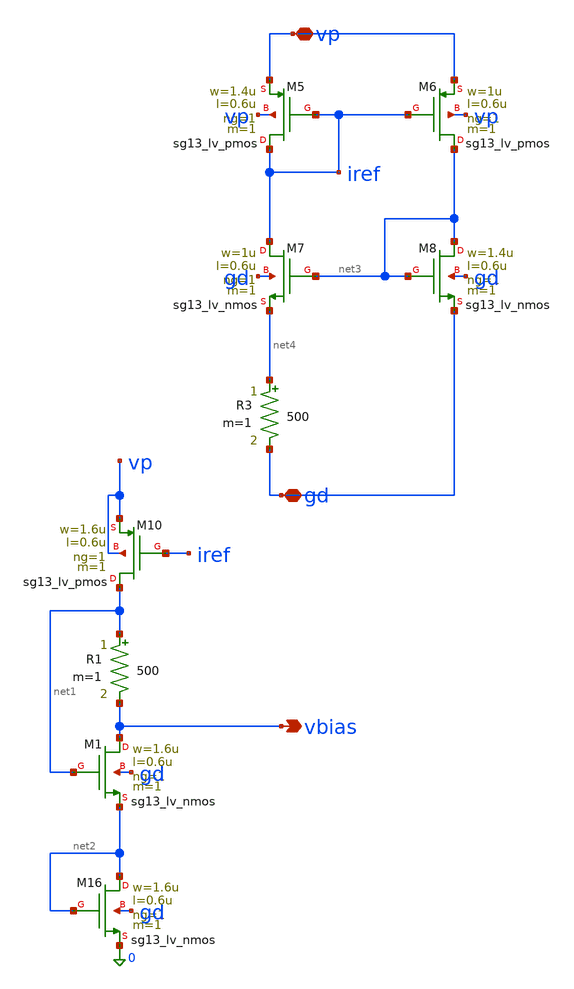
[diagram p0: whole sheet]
** sch_path: charge_pump/vbias_p.sch
**.subckt vbias_p vp gd vbias
*.iopin vp
*.iopin gd
*.opin vbias
XM16 net2 net2 0 gd sg13_lv_nmos w=1.6u l=0.6u ng=1 m=1 mm_ok=1
XM1 vbias net1 net2 gd sg13_lv_nmos w=1.6u l=0.6u ng=1 m=1 mm_ok=1
R1 net1 vbias 500 m=1
XM5 iref iref vp vp sg13_lv_pmos w=1.4u l=0.6u ng=1 m=1 mm_ok=1
XM6 net3 iref vp vp sg13_lv_pmos w=1u l=0.6u ng=1 m=1 mm_ok=1
XM7 iref net3 net4 gd sg13_lv_nmos w=1u l=0.6u ng=1 m=1 mm_ok=1
XM8 net3 net3 gd gd sg13_lv_nmos w=1.4u l=0.6u ng=1 m=1 mm_ok=1
R3 net4 gd 500 m=1
XM10 net1 iref vp vp sg13_lv_pmos w=1.6u l=0.6u ng=1 m=1 mm_ok=1
**.ends
.end
